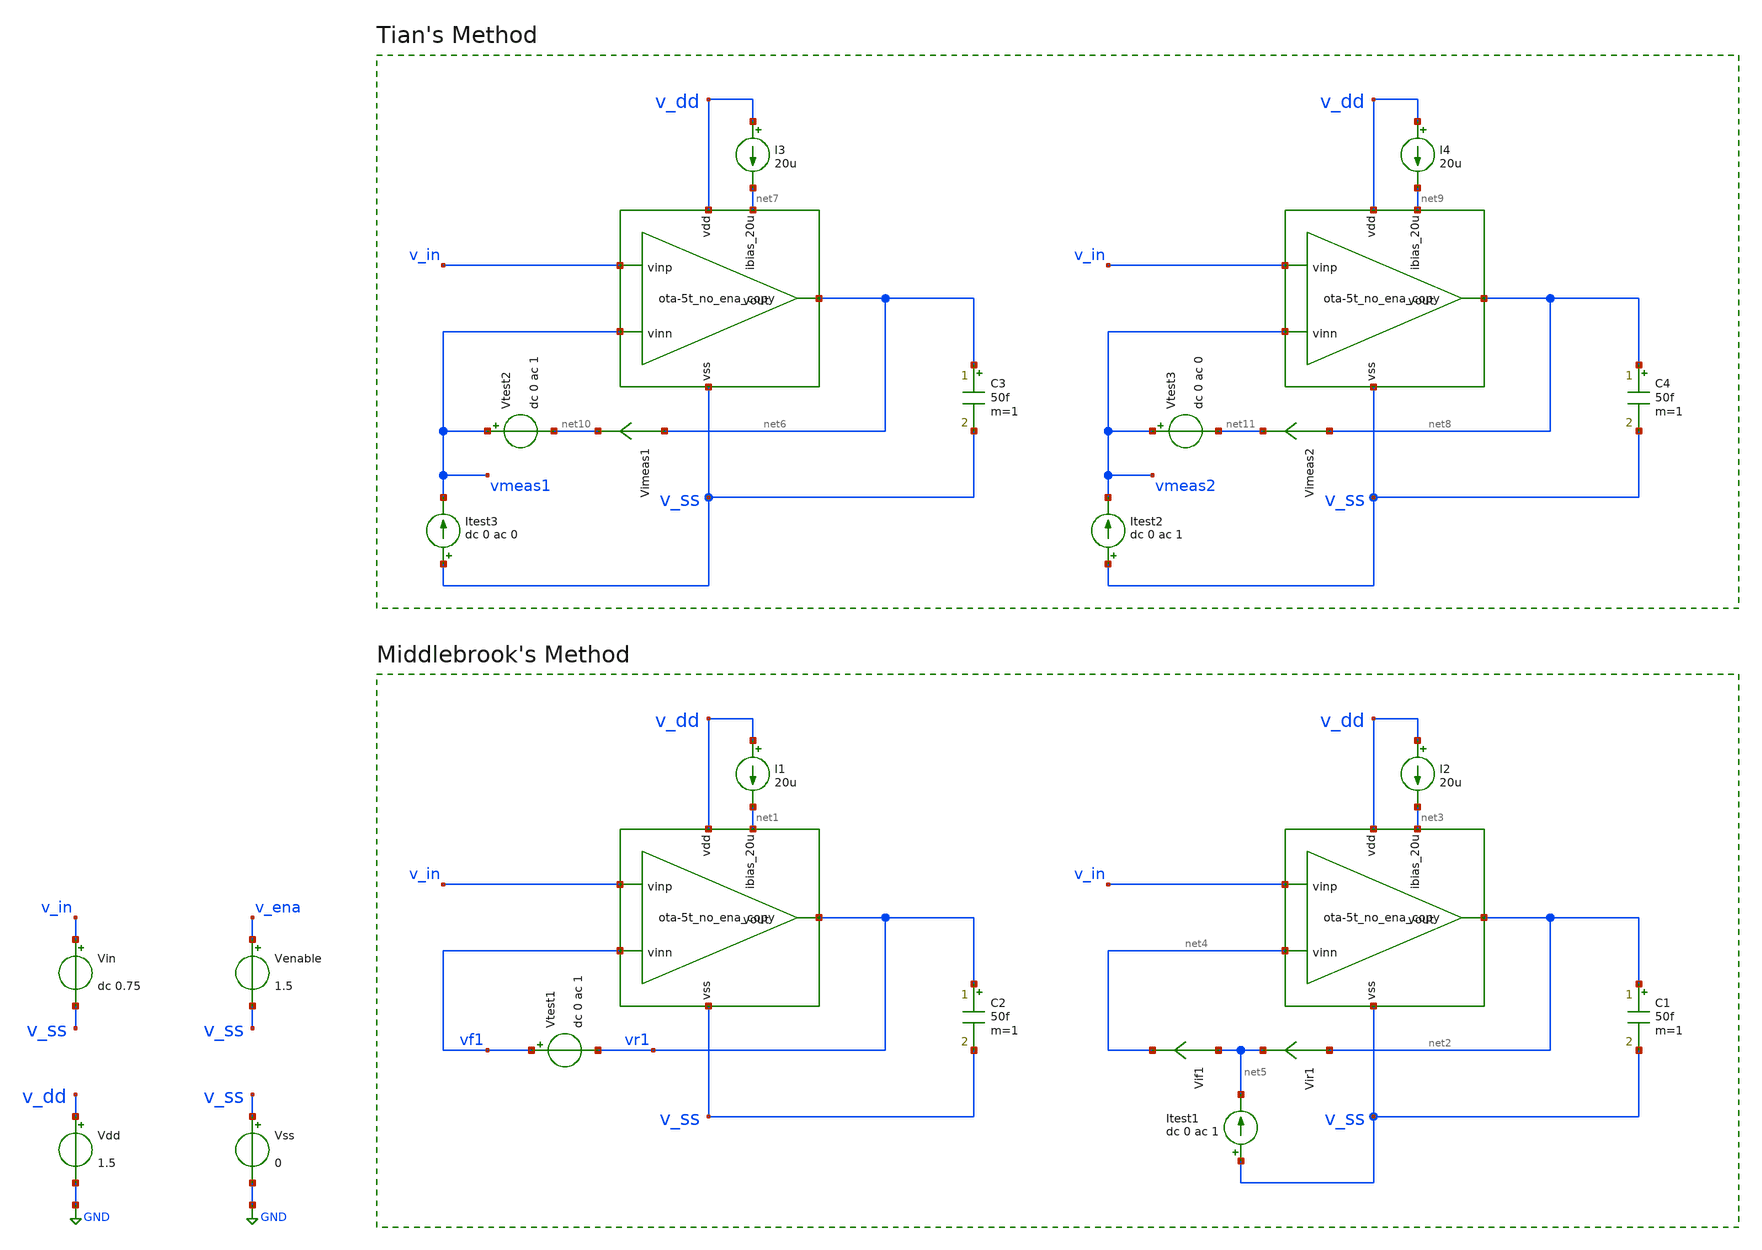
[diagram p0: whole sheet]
** sch_path: 004_Real_Circuits/003_version_second_output_stage/ota-5t_tb-loopgain_no_ena.sch
* (c) 2024-2025 H. Pretl, S. Dorrer, Apache-2.0 license
**.subckt ota-5t_tb-loopgain_no_ena
Vdd v_dd GND 1.5
Vss v_ss GND 0
Vin v_in v_ss dc 0.75
Venable v_ena v_ss 1.5
C2 vr1 v_ss 50f m=1
I1 v_dd net1 20u
Vtest1 vf1 vr1 dc 0 ac 1
C1 net2 v_ss 50f m=1
I2 v_dd net3 20u
Vir1 net2 net5 0
.save i(vir1)
Vif1 net5 net4 0
.save i(vif1)
Itest1 v_ss net5 dc 0 ac 1
C3 net6 v_ss 50f m=1
I3 v_dd net7 20u
C4 net8 v_ss 50f m=1
I4 v_dd net9 20u
Itest3 v_ss vmeas1 dc 0 ac 0
Vtest2 vmeas1 net10 dc 0 ac 1
Vimeas1 net6 net10 0
.save i(vimeas1)
Itest2 v_ss vmeas2 dc 0 ac 1
Vtest3 vmeas2 net11 dc 0 ac 0
Vimeas2 net8 net11 0
.save i(vimeas2)
x1 v_dd net6 v_in vmeas1 net7 v_ss ota-5t_no_ena_copy
x2 v_dd net8 v_in vmeas2 net9 v_ss ota-5t_no_ena_copy
x3 v_dd vr1 v_in vf1 net1 v_ss ota-5t_no_ena_copy
x4 v_dd net2 v_in net4 net3 v_ss ota-5t_no_ena_copy
**** begin user architecture code
 .lib cornerMOSlv.lib mos_tt



.param temp=27
.options savecurrents reltol=1e-3 abstol=1e-12 gmin=1e-15
.control
save all

* Operating Point Analysis
op
remzerovec
write ota-5t_tb-loopgain.raw
set appendwrite

* AC Analysis
ac dec 101 1 100G
remzerovec
write ota-5t_tb-loopgain.raw
set appendwrite

* Middlebrook's Method
let tv=-v(vr1)/v(vf1)
let ti=-i(vir1)/i(vif1)
let tmb=(tv*ti - 1)/(tv + ti + 2)

plot db(tmb) ylabel 'Magnitude - Middlebrook'
plot 180/pi*cphase(tmb) ylabel 'Phase - Middlebrook'

* Tian's Method
* vtest=0, itest=1:
let A=i(Vimeas2)
let C=v(vmeas2)

* vtest=1, itest=0:
let B=i(Vimeas1)
let D=v(vmeas1)
let ttian=(A*D-B*C-A)/(2*(B*C-A*D)+A-D+1)

plot db(ttian) ylabel 'Magnitude - Tian'
plot 180/pi*cphase(ttian) ylabel 'Phase - Tian'

* Middlebrook vs. Tian
plot db(tmb) db(ttian) ylabel 'Magnitude'
plot 180/pi*cphase(tmb) 180/pi*cphase(ttian) ylabel 'Phase'

write ota-5t_tb-loopgain.raw

*quit
.endc


**** end user architecture code
**.ends

* expanding   symbol:  004_Real_Circuits/003_version_second_output_stage/ota-5t_no_ena_copy.sym # of
*+ pins=6
** sym_path: 004_Real_Circuits/003_version_second_output_stage/ota-5t_no_ena_copy.sym
** sch_path: 004_Real_Circuits/003_version_second_output_stage/ota-5t_no_ena_copy.sch
.subckt ota-5t_no_ena_copy vdd vout vinp vinn ibias_20u vss
*.opin vout
*.iopin vdd
*.ipin vinp
*.ipin vinn
*.ipin ibias_20u
*.iopin vss
XM5 tail ibias_20u vss vss sg13_lv_nmos w=1.5u l=5u ng=1 m=1 mm_ok=1
XM4 net1 gate_p vdd vdd sg13_lv_pmos w=3.5u l=5u ng=1 m=1 mm_ok=1
XM1 gate_p vinn tail vss sg13_lv_nmos w=2u l=5u ng=1 m=1 mm_ok=1
XM2 net1 vinp tail vss sg13_lv_nmos w=2u l=5u ng=1 m=1 mm_ok=1
XM3 gate_p gate_p vdd vdd sg13_lv_pmos w=3.5u l=5u ng=1 m=1 mm_ok=1
XM6 ibias_20u ibias_20u vss vss sg13_lv_nmos w=10u l=5u ng=5 m=1 mm_ok=1
XM7 vout net1 vdd vdd sg13_lv_pmos w=8.5u l=5u ng=1 m=1 mm_ok=1
XM8 vout ibias_20u vss vss sg13_lv_nmos w=0.75u l=5u ng=1 m=1 mm_ok=1
C2 net2 vout 795f m=1
R1 net1 net2 59k m=1
.ends

.GLOBAL GND
.end
